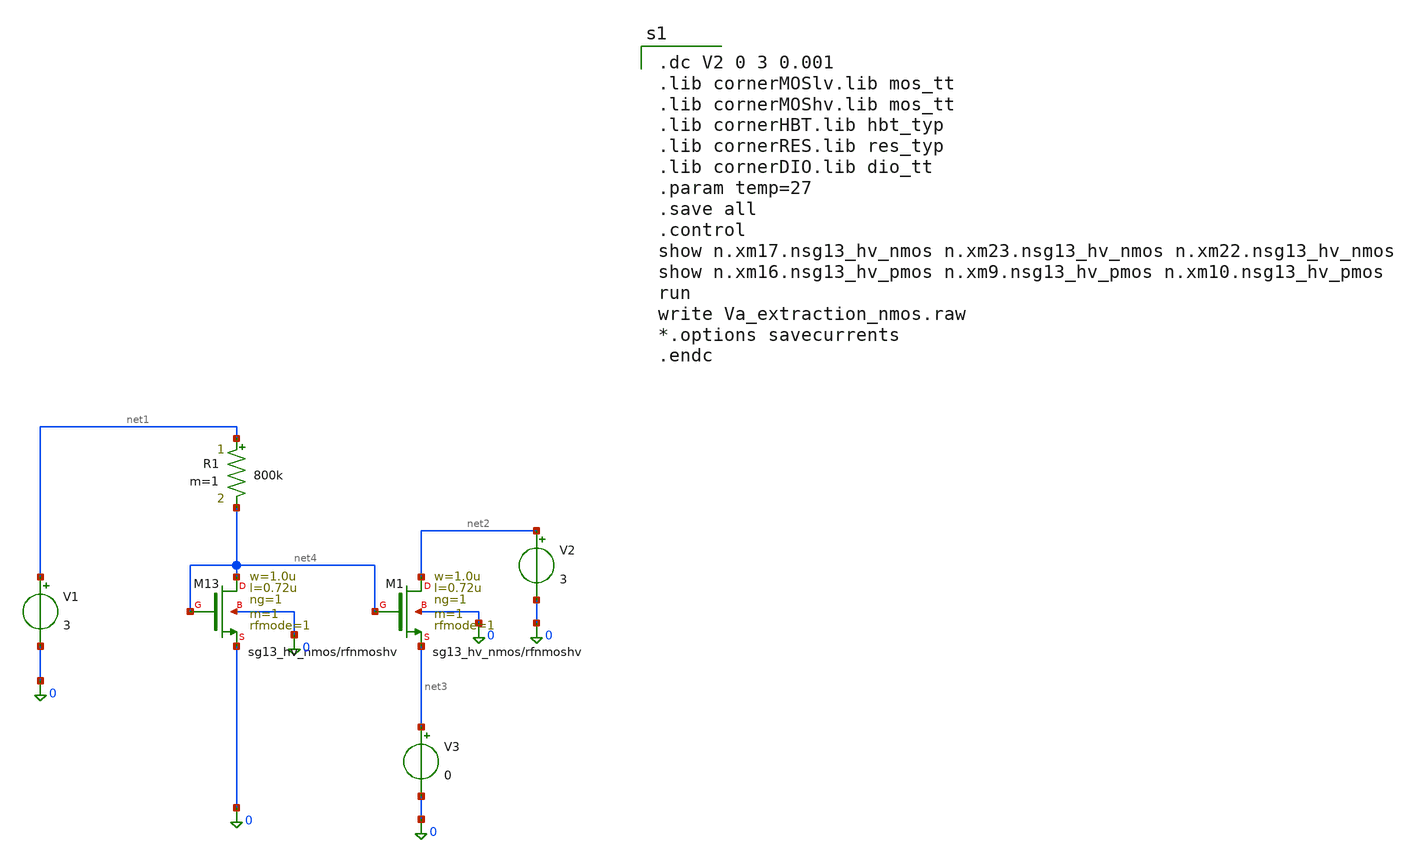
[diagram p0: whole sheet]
** sch_path: src/Va_extraction_nmos.sch
**.subckt Va_extraction_nmos
R1 net1 net4 800k m=1
V1 net1 0 3
V2 net2 0 3
V3 net3 0 0
XM13 net4 net4 0 0 sg13_hv_nmos w=1.0u l=0.72u ng=1 m=1 rfmode=1 mm_ok=1
XM1 net2 net4 net3 0 sg13_hv_nmos w=1.0u l=0.72u ng=1 m=1 rfmode=1 mm_ok=1
**** begin user architecture code

.dc V2 0 3 0.001
.lib cornerMOSlv.lib mos_tt
.lib cornerMOShv.lib mos_tt
.lib cornerHBT.lib hbt_typ
.lib cornerRES.lib res_typ
.lib cornerDIO.lib dio_tt
.param temp=27
.save all
.control
show n.xm17.nsg13_hv_nmos n.xm23.nsg13_hv_nmos n.xm22.nsg13_hv_nmos
show n.xm16.nsg13_hv_pmos n.xm9.nsg13_hv_pmos n.xm10.nsg13_hv_pmos
run
write Va_extraction_nmos.raw
*.options savecurrents
.endc

**** end user architecture code
**.ends
.end
